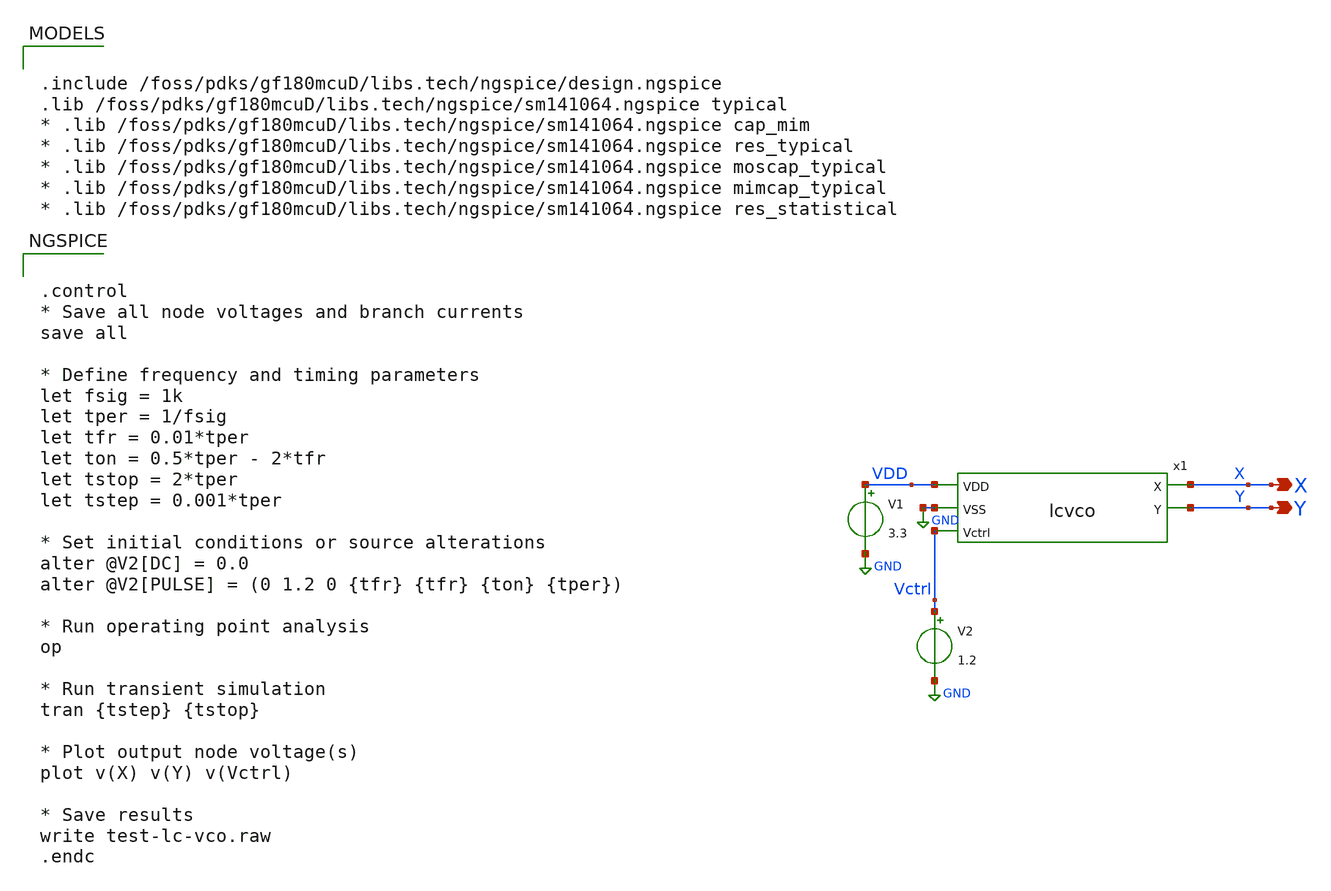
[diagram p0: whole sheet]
** sch_path: Project/1-on-chip/schematic/VCO/test-lc-vco.sch
**.subckt test-lc-vco X Y
*.opin X
*.opin Y
V1 VDD GND 3.3
V2 Vctrl GND 1.2
x1 VDD X Y GND Vctrl lcvco
**** begin user architecture code

.include /foss/pdks/gf180mcuD/libs.tech/ngspice/design.ngspice
.lib /foss/pdks/gf180mcuD/libs.tech/ngspice/sm141064.ngspice typical
* .lib /foss/pdks/gf180mcuD/libs.tech/ngspice/sm141064.ngspice cap_mim
* .lib /foss/pdks/gf180mcuD/libs.tech/ngspice/sm141064.ngspice res_typical
* .lib /foss/pdks/gf180mcuD/libs.tech/ngspice/sm141064.ngspice moscap_typical
* .lib /foss/pdks/gf180mcuD/libs.tech/ngspice/sm141064.ngspice mimcap_typical
* .lib /foss/pdks/gf180mcuD/libs.tech/ngspice/sm141064.ngspice res_statistical



.control
* Save all node voltages and branch currents
save all

* Define frequency and timing parameters
let fsig = 1k
let tper = 1/fsig
let tfr = 0.01*tper
let ton = 0.5*tper - 2*tfr
let tstop = 2*tper
let tstep = 0.001*tper

* Set initial conditions or source alterations
alter @V2[DC] = 0.0
alter @V2[PULSE] = (0 1.2 0 {tfr} {tfr} {ton} {tper})

* Run operating point analysis
op

* Run transient simulation
tran {tstep} {tstop}

* Plot output node voltage(s)
plot v(X) v(Y) v(Vctrl)

* Save results
write test-lc-vco.raw
.endc



**** end user architecture code
**.ends

* expanding   symbol:  gf180mcuD/lc-vco/lcvco.sym # of pins=5
** sym_path: Project/1-on-chip/schematic/VCO/lcvco.sym
** sch_path: Project/1-on-chip/schematic/VCO/lcvco.sch
.subckt lcvco VDD X Y VSS Vctrl
*.ipin VDD
*.ipin Vctrl
*.opin X
*.opin Y
*.ipin VSS
XM1 Y X net1 VSS nfet_03v3 L=60n W=60u nf=1 ad='int((nf+1)/2) * W/nf * 0.18u' as='int((nf+2)/2) * W/nf * 0.18u'
+ pd='2*int((nf+1)/2) * (W/nf + 0.18u)' ps='2*int((nf+2)/2) * (W/nf + 0.18u)' nrd='0.18u / W' nrs='0.18u / W'
+ sa=0 sb=0 sd=0 m=1
XM2 X Y VDD VDD pfet_03v3 L=60n W=120u nf=1 ad='int((nf+1)/2) * W/nf * 0.18u' as='int((nf+2)/2) * W/nf * 0.18u'
+ pd='2*int((nf+1)/2) * (W/nf + 0.18u)' ps='2*int((nf+2)/2) * (W/nf + 0.18u)' nrd='0.18u / W' nrs='0.18u / W'
+ sa=0 sb=0 sd=0 m=1
XM3 Y X VDD VDD pfet_03v3 L=60n W=120u nf=1 ad='int((nf+1)/2) * W/nf * 0.18u' as='int((nf+2)/2) * W/nf * 0.18u'
+ pd='2*int((nf+1)/2) * (W/nf + 0.18u)' ps='2*int((nf+2)/2) * (W/nf + 0.18u)' nrd='0.18u / W' nrs='0.18u / W'
+ sa=0 sb=0 sd=0 m=1
XM4 X Y net1 VSS nfet_03v3 L=60n W=60u nf=1 ad='int((nf+1)/2) * W/nf * 0.18u' as='int((nf+2)/2) * W/nf * 0.18u'
+ pd='2*int((nf+1)/2) * (W/nf + 0.18u)' ps='2*int((nf+2)/2) * (W/nf + 0.18u)' nrd='0.18u / W' nrs='0.18u / W'
+ sa=0 sb=0 sd=0 m=1
XM5 Vctrl X Vctrl VSS nfet_03v3 L=2.86u W=50u nf=1 ad='int((nf+1)/2) * W/nf * 0.18u' as='int((nf+2)/2) * W/nf * 0.18u'
+ pd='2*int((nf+1)/2) * (W/nf + 0.18u)' ps='2*int((nf+2)/2) * (W/nf + 0.18u)' nrd='0.18u / W' nrs='0.18u / W'
+ sa=0 sb=0 sd=0 m=1
XM6 Vctrl Y Vctrl VSS nfet_03v3 L=2.86u W=50u nf=1 ad='int((nf+1)/2) * W/nf * 0.18u' as='int((nf+2)/2) * W/nf * 0.18u'
+ pd='2*int((nf+1)/2) * (W/nf + 0.18u)' ps='2*int((nf+2)/2) * (W/nf + 0.18u)' nrd='0.18u / W' nrs='0.18u / W'
+ sa=0 sb=0 sd=0 m=1
L1 Y X 2.5n m=1
L2 net1 VSS 10n m=1
C1 Y X 1p m=1
.ends

.GLOBAL GND
.end
